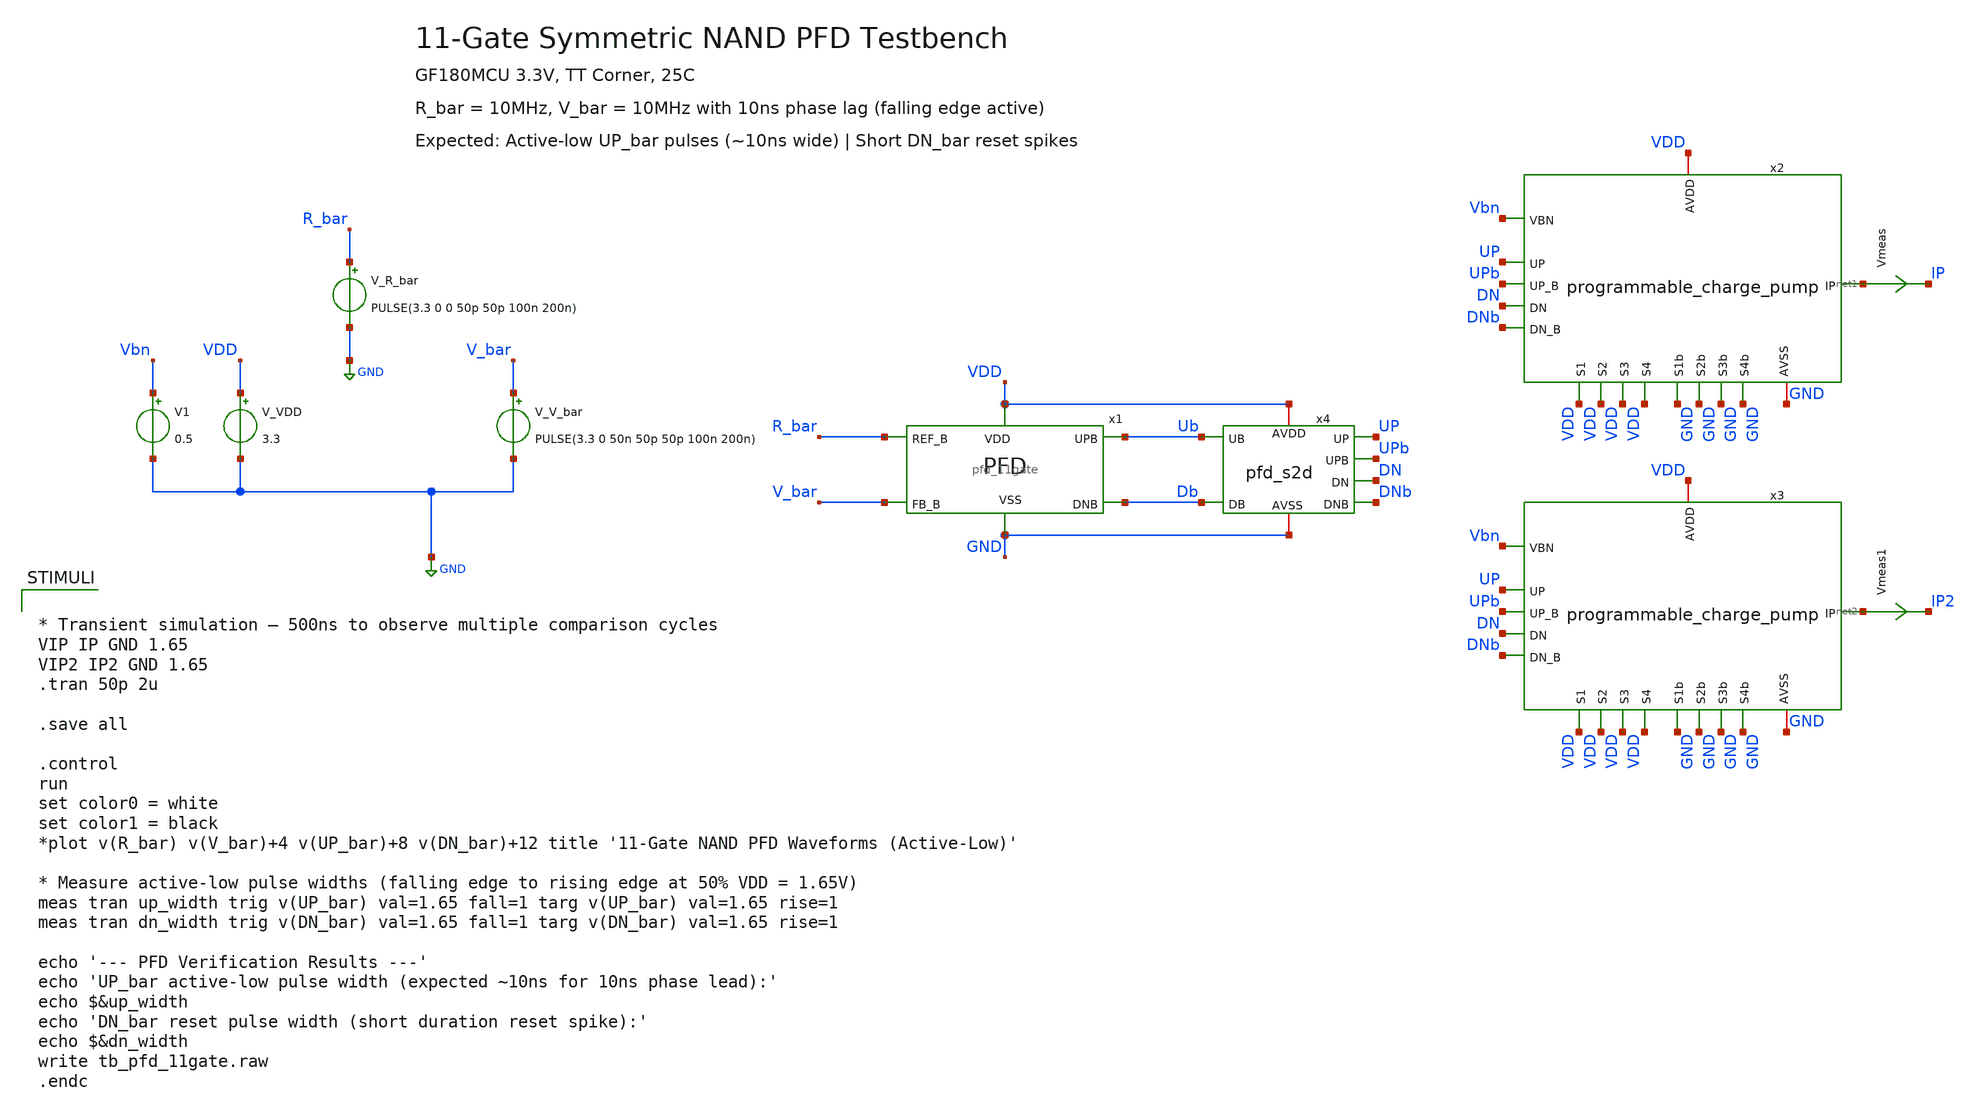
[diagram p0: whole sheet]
** sch_path: designs/libs/tb_analog/tb_pfd/ys_tb_pfd_11gate.sch
**.subckt ys_tb_pfd_11gate
V_R_bar R_bar GND PULSE(3.3 0 0 50p 50p 100n 200n)
V_V_bar V_bar GND PULSE(3.3 0 50n 50p 50p 100n 200n)
V_VDD VDD GND 3.3
x1 R_bar Ub Db V_bar VDD GND pfd_11gate
x2 GND VDD UP UPb DN net1 DNb Vbn GND VDD GND VDD GND VDD GND VDD programmable_charge_pump
V1 Vbn GND 0.5
Vmeas net1 IP 0
.save i(vmeas)
x3 GND VDD UP UPb DN net2 DNb Vbn GND VDD GND VDD GND VDD GND VDD programmable_charge_pump
Vmeas1 net2 IP2 0
.save i(vmeas1)
x4 UPb Ub UP VDD GND DNb Db DN pfd_s2d
**** begin user architecture code


* Transient simulation — 500ns to observe multiple comparison cycles
VIP IP GND 1.65
VIP2 IP2 GND 1.65
.tran 50p 2u

.save all

.control
run
set color0 = white
set color1 = black
*plot v(R_bar) v(V_bar)+4 v(UP_bar)+8 v(DN_bar)+12 title '11-Gate NAND PFD Waveforms (Active-Low)'

* Measure active-low pulse widths (falling edge to rising edge at 50% VDD = 1.65V)
meas tran up_width trig v(UP_bar) val=1.65 fall=1 targ v(UP_bar) val=1.65 rise=1
meas tran dn_width trig v(DN_bar) val=1.65 fall=1 targ v(DN_bar) val=1.65 rise=1

echo '--- PFD Verification Results ---'
echo 'UP_bar active-low pulse width (expected ~10ns for 10ns phase lead):'
echo $&up_width
echo 'DN_bar reset pulse width (short duration reset spike):'
echo $&dn_width
write tb_pfd_11gate.raw
.endc



.include /foss/pdks/ciel/gf180mcu/versions/7b70722e33c03fcb5dabcf4d479fb0822d9251c9/gf180mcuD/libs.ref/gf180mcu_fd_sc_mcu7t5v0/spice/gf180mcu_fd_sc_mcu7t5v0.spice
.include $::180MCU_MODELS/design.ngspice
.lib $::180MCU_MODELS/sm141064.ngspice typical

**** end user architecture code
**.ends
.GLOBAL GND
.end
